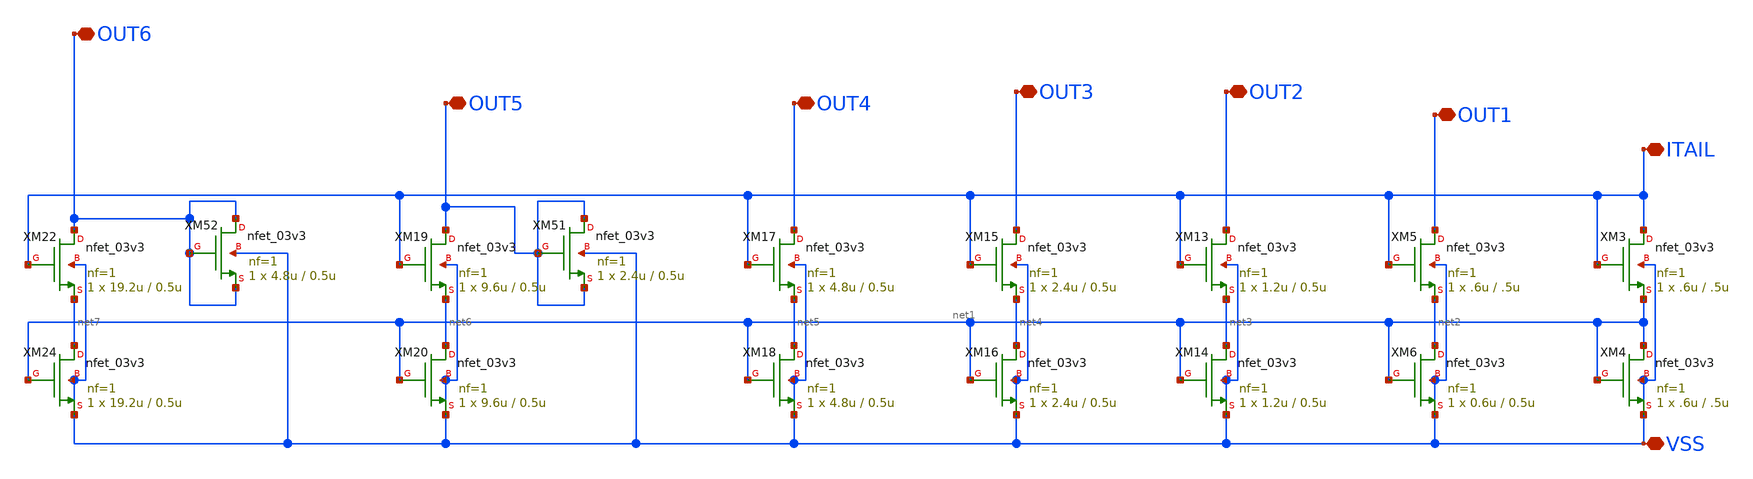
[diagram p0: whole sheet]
** sch_path: DAC_PAKISTAN_01/Pakistan1_Xschem/CM_LSB_V1.sch
**.subckt CM_LSB_V1 ITAIL VSS OUT1 OUT2 OUT3 OUT4 OUT5 OUT6
*.iopin ITAIL
*.iopin VSS
*.iopin OUT1
*.iopin OUT2
*.iopin OUT3
*.iopin OUT4
*.iopin OUT5
*.iopin OUT6
XM3 ITAIL ITAIL net1 VSS nfet_03v3 L=.5u W=.6u nf=1 ad='int((nf+1)/2) * W/nf * 0.18u' as='int((nf+2)/2) * W/nf * 0.18u'
+ pd='2*int((nf+1)/2) * (W/nf + 0.18u)' ps='2*int((nf+2)/2) * (W/nf + 0.18u)' nrd='0.18u / W' nrs='0.18u / W'
+ sa=0 sb=0 sd=0 m=1
XM4 net1 net1 VSS VSS nfet_03v3 L=.5u W=.6u nf=1 ad='int((nf+1)/2) * W/nf * 0.18u' as='int((nf+2)/2) * W/nf * 0.18u'
+ pd='2*int((nf+1)/2) * (W/nf + 0.18u)' ps='2*int((nf+2)/2) * (W/nf + 0.18u)' nrd='0.18u / W' nrs='0.18u / W'
+ sa=0 sb=0 sd=0 m=1
XM5 OUT1 ITAIL net2 VSS nfet_03v3 L=.5u W=.6u nf=1 ad='int((nf+1)/2) * W/nf * 0.18u' as='int((nf+2)/2) * W/nf * 0.18u'
+ pd='2*int((nf+1)/2) * (W/nf + 0.18u)' ps='2*int((nf+2)/2) * (W/nf + 0.18u)' nrd='0.18u / W' nrs='0.18u / W'
+ sa=0 sb=0 sd=0 m=1
XM6 net2 net1 VSS VSS nfet_03v3 L=0.5u W=0.6u nf=1 ad='int((nf+1)/2) * W/nf * 0.18u' as='int((nf+2)/2) * W/nf * 0.18u'
+ pd='2*int((nf+1)/2) * (W/nf + 0.18u)' ps='2*int((nf+2)/2) * (W/nf + 0.18u)' nrd='0.18u / W' nrs='0.18u / W'
+ sa=0 sb=0 sd=0 m=1
XM13 OUT2 ITAIL net3 VSS nfet_03v3 L=0.5u W=1.2u nf=1 ad='int((nf+1)/2) * W/nf * 0.18u' as='int((nf+2)/2) * W/nf * 0.18u'
+ pd='2*int((nf+1)/2) * (W/nf + 0.18u)' ps='2*int((nf+2)/2) * (W/nf + 0.18u)' nrd='0.18u / W' nrs='0.18u / W'
+ sa=0 sb=0 sd=0 m=1
XM14 net3 net1 VSS VSS nfet_03v3 L=0.5u W=1.2u nf=1 ad='int((nf+1)/2) * W/nf * 0.18u' as='int((nf+2)/2) * W/nf * 0.18u'
+ pd='2*int((nf+1)/2) * (W/nf + 0.18u)' ps='2*int((nf+2)/2) * (W/nf + 0.18u)' nrd='0.18u / W' nrs='0.18u / W'
+ sa=0 sb=0 sd=0 m=1
XM15 OUT3 ITAIL net4 VSS nfet_03v3 L=0.5u W=2.4u nf=1 ad='int((nf+1)/2) * W/nf * 0.18u' as='int((nf+2)/2) * W/nf * 0.18u'
+ pd='2*int((nf+1)/2) * (W/nf + 0.18u)' ps='2*int((nf+2)/2) * (W/nf + 0.18u)' nrd='0.18u / W' nrs='0.18u / W'
+ sa=0 sb=0 sd=0 m=1
XM16 net4 net1 VSS VSS nfet_03v3 L=0.5u W=2.4u nf=1 ad='int((nf+1)/2) * W/nf * 0.18u' as='int((nf+2)/2) * W/nf * 0.18u'
+ pd='2*int((nf+1)/2) * (W/nf + 0.18u)' ps='2*int((nf+2)/2) * (W/nf + 0.18u)' nrd='0.18u / W' nrs='0.18u / W'
+ sa=0 sb=0 sd=0 m=1
XM17 OUT4 ITAIL net5 VSS nfet_03v3 L=0.5u W=4.8u nf=1 ad='int((nf+1)/2) * W/nf * 0.18u' as='int((nf+2)/2) * W/nf * 0.18u'
+ pd='2*int((nf+1)/2) * (W/nf + 0.18u)' ps='2*int((nf+2)/2) * (W/nf + 0.18u)' nrd='0.18u / W' nrs='0.18u / W'
+ sa=0 sb=0 sd=0 m=1
XM18 net5 net1 VSS VSS nfet_03v3 L=0.5u W=4.8u nf=1 ad='int((nf+1)/2) * W/nf * 0.18u' as='int((nf+2)/2) * W/nf * 0.18u'
+ pd='2*int((nf+1)/2) * (W/nf + 0.18u)' ps='2*int((nf+2)/2) * (W/nf + 0.18u)' nrd='0.18u / W' nrs='0.18u / W'
+ sa=0 sb=0 sd=0 m=1
XM19 OUT5 ITAIL net6 VSS nfet_03v3 L=0.5u W=9.6u nf=1 ad='int((nf+1)/2) * W/nf * 0.18u' as='int((nf+2)/2) * W/nf * 0.18u'
+ pd='2*int((nf+1)/2) * (W/nf + 0.18u)' ps='2*int((nf+2)/2) * (W/nf + 0.18u)' nrd='0.18u / W' nrs='0.18u / W'
+ sa=0 sb=0 sd=0 m=1
XM20 net6 net1 VSS VSS nfet_03v3 L=0.5u W=9.6u nf=1 ad='int((nf+1)/2) * W/nf * 0.18u' as='int((nf+2)/2) * W/nf * 0.18u'
+ pd='2*int((nf+1)/2) * (W/nf + 0.18u)' ps='2*int((nf+2)/2) * (W/nf + 0.18u)' nrd='0.18u / W' nrs='0.18u / W'
+ sa=0 sb=0 sd=0 m=1
XM22 OUT6 ITAIL net7 VSS nfet_03v3 L=0.5u W=19.2u nf=1 ad='int((nf+1)/2) * W/nf * 0.18u' as='int((nf+2)/2) * W/nf * 0.18u'
+ pd='2*int((nf+1)/2) * (W/nf + 0.18u)' ps='2*int((nf+2)/2) * (W/nf + 0.18u)' nrd='0.18u / W' nrs='0.18u / W'
+ sa=0 sb=0 sd=0 m=1
XM24 net7 net1 VSS VSS nfet_03v3 L=0.5u W=19.2u nf=1 ad='int((nf+1)/2) * W/nf * 0.18u' as='int((nf+2)/2) * W/nf * 0.18u'
+ pd='2*int((nf+1)/2) * (W/nf + 0.18u)' ps='2*int((nf+2)/2) * (W/nf + 0.18u)' nrd='0.18u / W' nrs='0.18u / W'
+ sa=0 sb=0 sd=0 m=1
XM51 OUT5 OUT5 OUT5 VSS nfet_03v3 L=0.5u W=2.4u nf=1 ad='int((nf+1)/2) * W/nf * 0.18u' as='int((nf+2)/2) * W/nf * 0.18u'
+ pd='2*int((nf+1)/2) * (W/nf + 0.18u)' ps='2*int((nf+2)/2) * (W/nf + 0.18u)' nrd='0.18u / W' nrs='0.18u / W'
+ sa=0 sb=0 sd=0 m=1
XM52 OUT6 OUT6 OUT6 VSS nfet_03v3 L=0.5u W=4.8u nf=1 ad='int((nf+1)/2) * W/nf * 0.18u' as='int((nf+2)/2) * W/nf * 0.18u'
+ pd='2*int((nf+1)/2) * (W/nf + 0.18u)' ps='2*int((nf+2)/2) * (W/nf + 0.18u)' nrd='0.18u / W' nrs='0.18u / W'
+ sa=0 sb=0 sd=0 m=1
**.ends
.end
